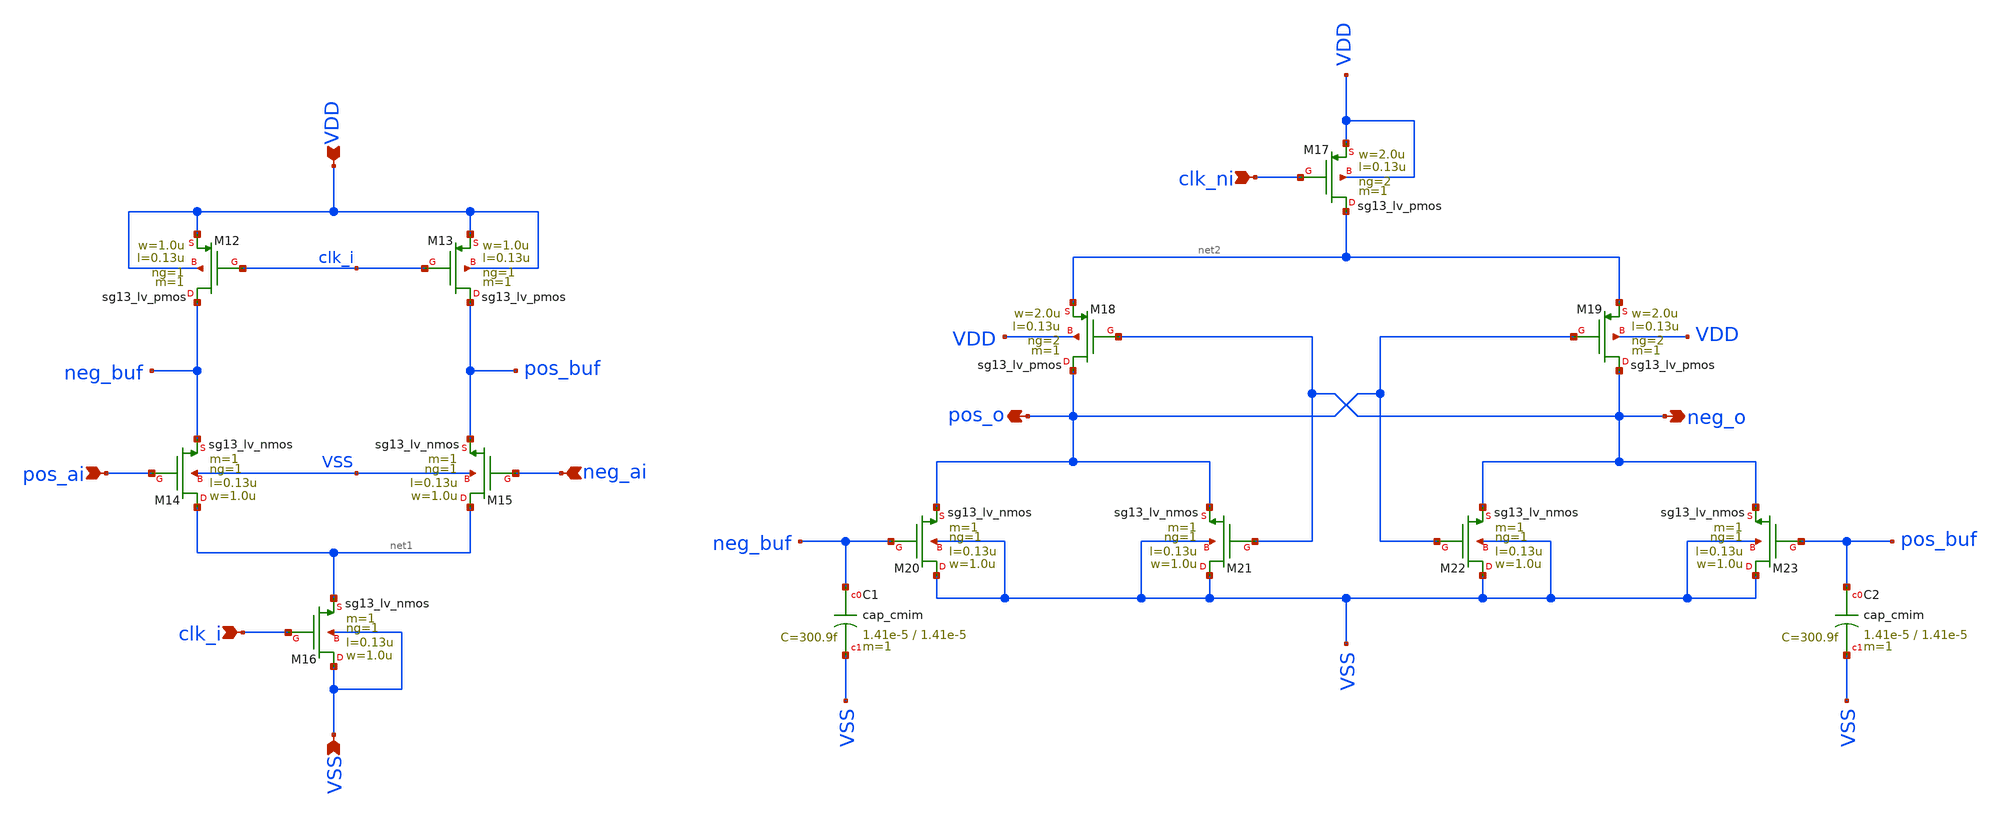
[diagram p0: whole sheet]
** sch_path: designs/comparator_dt/comparator.sch
**.subckt comparator pos_ai neg_ai VSS VDD neg_o pos_o clk_i clk_ni
*.ipin pos_ai
*.ipin neg_ai
*.ipin VSS
*.ipin VDD
*.opin neg_o
*.opin pos_o
*.ipin clk_i
*.ipin clk_ni
XM12 neg_buf clk_i VDD VDD sg13_lv_pmos w=1.0u l=0.13u ng=1 m=1 mm_ok=1
XM13 pos_buf clk_i VDD VDD sg13_lv_pmos w=1.0u l=0.13u ng=1 m=1 mm_ok=1
XM14 net1 pos_ai neg_buf VSS sg13_lv_nmos w=1.0u l=0.13u ng=1 m=1 mm_ok=1
XM15 net1 neg_ai pos_buf VSS sg13_lv_nmos w=1.0u l=0.13u ng=1 m=1 mm_ok=1
XM16 VSS clk_i net1 VSS sg13_lv_nmos w=1.0u l=0.13u ng=1 m=1 mm_ok=1
XM17 net2 clk_ni VDD VDD sg13_lv_pmos w=2.0u l=0.13u ng=2 m=1 mm_ok=1
XM18 pos_o neg_o net2 VDD sg13_lv_pmos w=2.0u l=0.13u ng=2 m=1 mm_ok=1
XM19 neg_o pos_o net2 VDD sg13_lv_pmos w=2.0u l=0.13u ng=2 m=1 mm_ok=1
XM20 VSS neg_buf pos_o VSS sg13_lv_nmos w=1.0u l=0.13u ng=1 m=1 mm_ok=1
XM21 VSS neg_o pos_o VSS sg13_lv_nmos w=1.0u l=0.13u ng=1 m=1 mm_ok=1
XM22 VSS pos_o neg_o VSS sg13_lv_nmos w=1.0u l=0.13u ng=1 m=1 mm_ok=1
XM23 VSS pos_buf neg_o VSS sg13_lv_nmos w=1.0u l=0.13u ng=1 m=1 mm_ok=1
XC1 neg_buf VSS cap_cmim w=1.41e-5 l=1.41e-5 m=1 mm_ok=1
XC2 pos_buf VSS cap_cmim w=1.41e-5 l=1.41e-5 m=1 mm_ok=1
**.ends
.end
